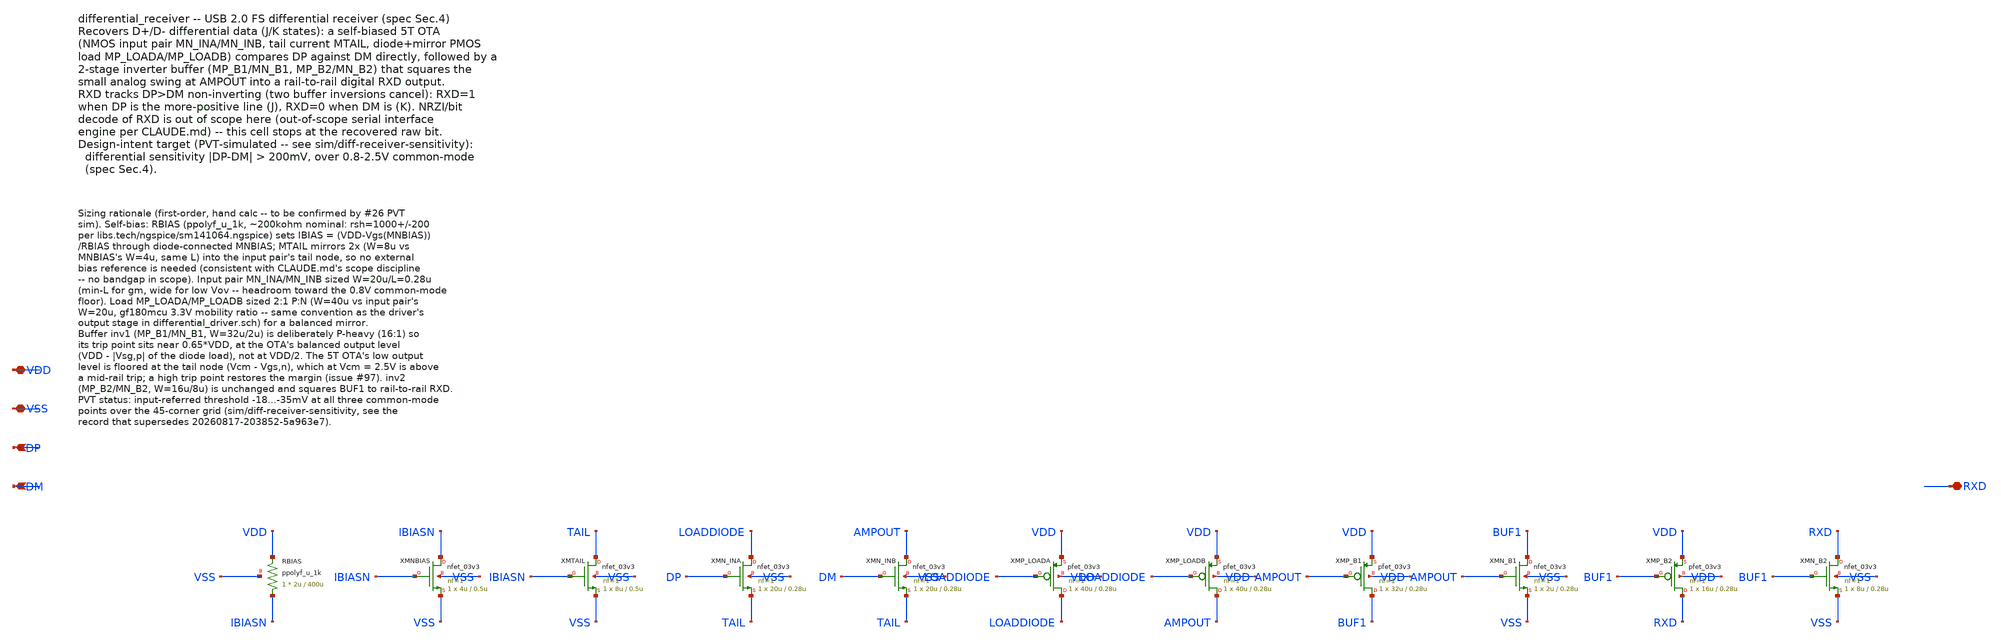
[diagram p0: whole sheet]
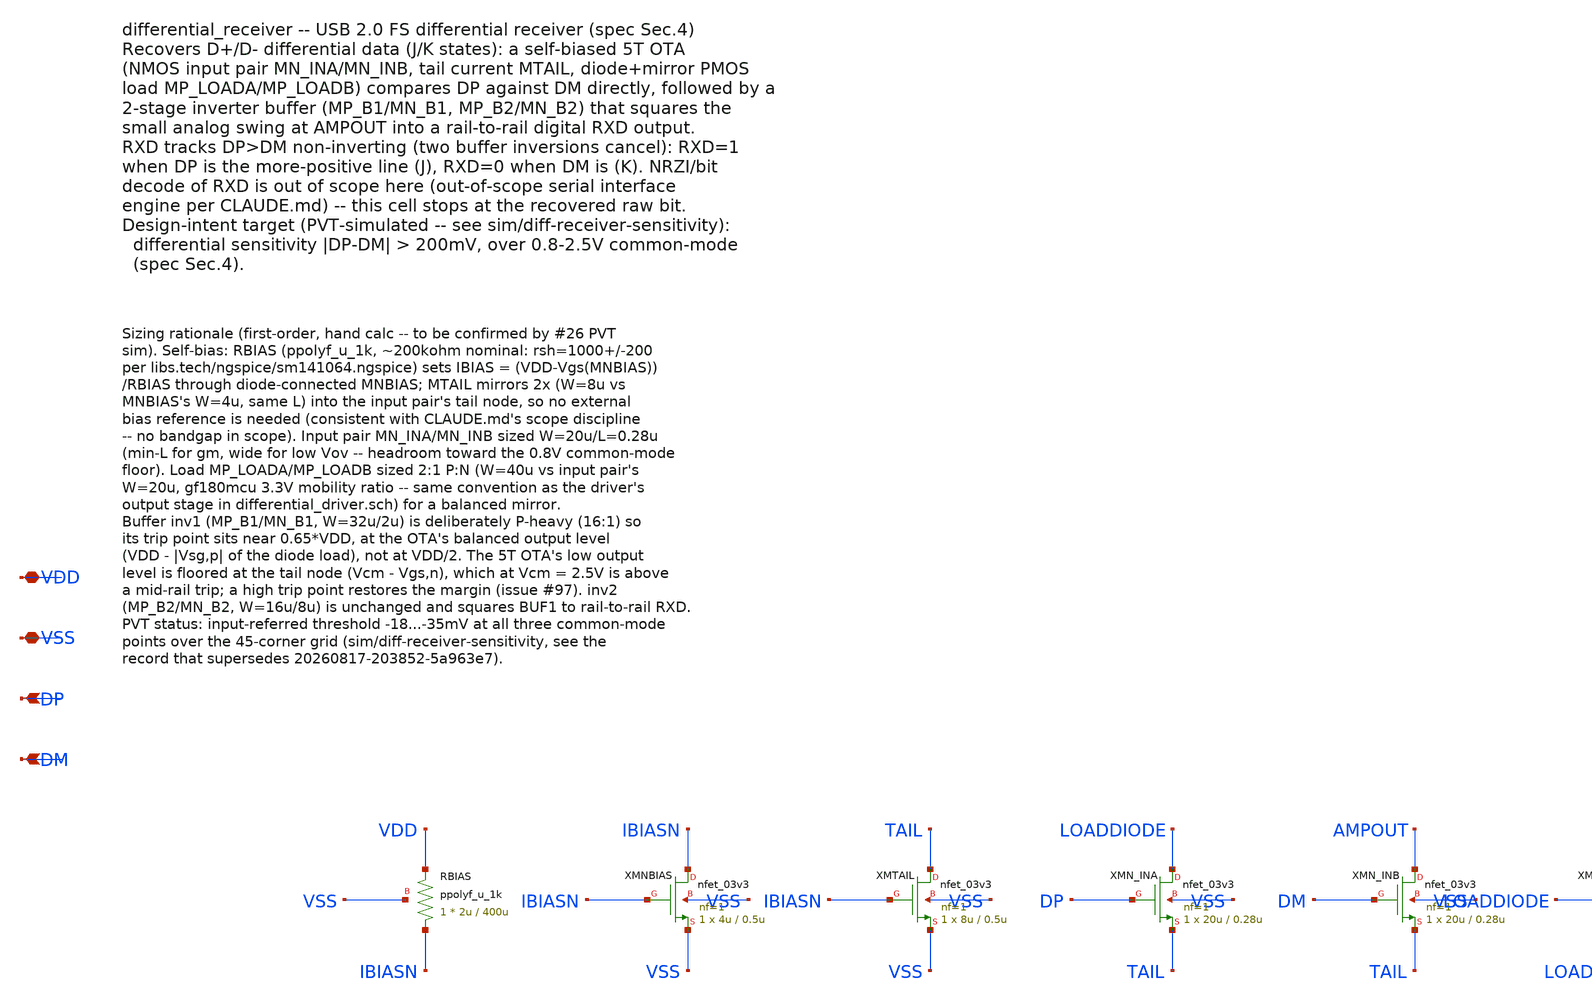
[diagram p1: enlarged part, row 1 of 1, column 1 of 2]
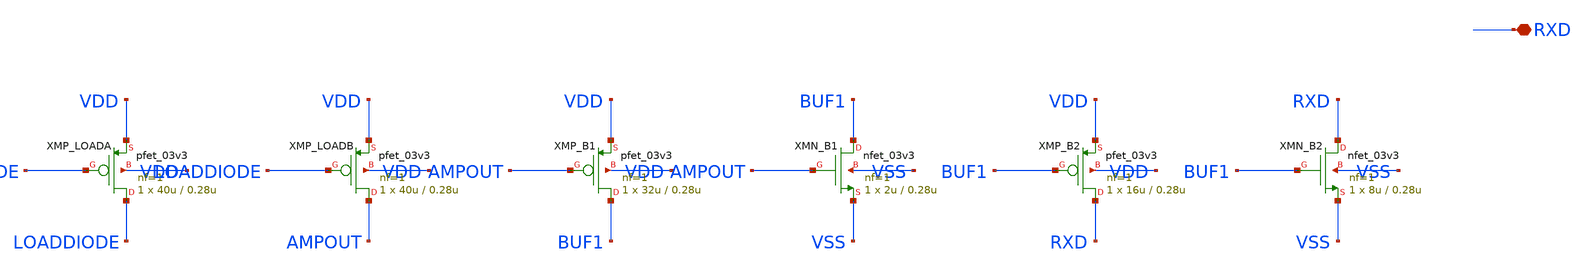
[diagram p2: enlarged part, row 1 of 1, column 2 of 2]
** sch_path: design/differential_receiver.sch
**.subckt differential_receiver VDD VSS DP DM RXD
*.iopin VDD
*.iopin VSS
*.ipin DP
*.ipin DM
*.iopin RXD
XRBIAS IBIASN VDD VSS ppolyf_u_1k r_width=2u r_length=400u m=1
XMNBIAS IBIASN IBIASN VSS VSS nfet_03v3 L=0.5u W=4u nf=1 ad='int((nf+1)/2) * W/nf * 0.18u' as='int((nf+2)/2) * W/nf * 0.18u'
+ pd='2*int((nf+1)/2) * (W/nf + 0.18u)' ps='2*int((nf+2)/2) * (W/nf + 0.18u)' nrd='0.18u / W' nrs='0.18u / W'
+ sa=0 sb=0 sd=0 m=1
XMTAIL TAIL IBIASN VSS VSS nfet_03v3 L=0.5u W=8u nf=1 ad='int((nf+1)/2) * W/nf * 0.18u' as='int((nf+2)/2) * W/nf * 0.18u'
+ pd='2*int((nf+1)/2) * (W/nf + 0.18u)' ps='2*int((nf+2)/2) * (W/nf + 0.18u)' nrd='0.18u / W' nrs='0.18u / W'
+ sa=0 sb=0 sd=0 m=1
XMN_INA LOADDIODE DP TAIL VSS nfet_03v3 L=0.28u W=20u nf=1 ad='int((nf+1)/2) * W/nf * 0.18u' as='int((nf+2)/2) * W/nf * 0.18u'
+ pd='2*int((nf+1)/2) * (W/nf + 0.18u)' ps='2*int((nf+2)/2) * (W/nf + 0.18u)' nrd='0.18u / W' nrs='0.18u / W'
+ sa=0 sb=0 sd=0 m=1
XMN_INB AMPOUT DM TAIL VSS nfet_03v3 L=0.28u W=20u nf=1 ad='int((nf+1)/2) * W/nf * 0.18u' as='int((nf+2)/2) * W/nf * 0.18u'
+ pd='2*int((nf+1)/2) * (W/nf + 0.18u)' ps='2*int((nf+2)/2) * (W/nf + 0.18u)' nrd='0.18u / W' nrs='0.18u / W'
+ sa=0 sb=0 sd=0 m=1
XMP_LOADA LOADDIODE LOADDIODE VDD VDD pfet_03v3 L=0.28u W=40u nf=1 ad='int((nf+1)/2) * W/nf * 0.18u'
+ as='int((nf+2)/2) * W/nf * 0.18u' pd='2*int((nf+1)/2) * (W/nf + 0.18u)' ps='2*int((nf+2)/2) * (W/nf + 0.18u)'
+ nrd='0.18u / W' nrs='0.18u / W' sa=0 sb=0 sd=0 m=1
XMP_LOADB AMPOUT LOADDIODE VDD VDD pfet_03v3 L=0.28u W=40u nf=1 ad='int((nf+1)/2) * W/nf * 0.18u' as='int((nf+2)/2) * W/nf * 0.18u'
+ pd='2*int((nf+1)/2) * (W/nf + 0.18u)' ps='2*int((nf+2)/2) * (W/nf + 0.18u)' nrd='0.18u / W' nrs='0.18u / W'
+ sa=0 sb=0 sd=0 m=1
XMP_B1 BUF1 AMPOUT VDD VDD pfet_03v3 L=0.28u W=32u nf=1 ad='int((nf+1)/2) * W/nf * 0.18u' as='int((nf+2)/2) * W/nf * 0.18u'
+ pd='2*int((nf+1)/2) * (W/nf + 0.18u)' ps='2*int((nf+2)/2) * (W/nf + 0.18u)' nrd='0.18u / W' nrs='0.18u / W'
+ sa=0 sb=0 sd=0 m=1
XMN_B1 BUF1 AMPOUT VSS VSS nfet_03v3 L=0.28u W=2u nf=1 ad='int((nf+1)/2) * W/nf * 0.18u' as='int((nf+2)/2) * W/nf * 0.18u'
+ pd='2*int((nf+1)/2) * (W/nf + 0.18u)' ps='2*int((nf+2)/2) * (W/nf + 0.18u)' nrd='0.18u / W' nrs='0.18u / W'
+ sa=0 sb=0 sd=0 m=1
XMP_B2 RXD BUF1 VDD VDD pfet_03v3 L=0.28u W=16u nf=1 ad='int((nf+1)/2) * W/nf * 0.18u' as='int((nf+2)/2) * W/nf * 0.18u'
+ pd='2*int((nf+1)/2) * (W/nf + 0.18u)' ps='2*int((nf+2)/2) * (W/nf + 0.18u)' nrd='0.18u / W' nrs='0.18u / W'
+ sa=0 sb=0 sd=0 m=1
XMN_B2 RXD BUF1 VSS VSS nfet_03v3 L=0.28u W=8u nf=1 ad='int((nf+1)/2) * W/nf * 0.18u' as='int((nf+2)/2) * W/nf * 0.18u'
+ pd='2*int((nf+1)/2) * (W/nf + 0.18u)' ps='2*int((nf+2)/2) * (W/nf + 0.18u)' nrd='0.18u / W' nrs='0.18u / W'
+ sa=0 sb=0 sd=0 m=1
**.ends
.end
